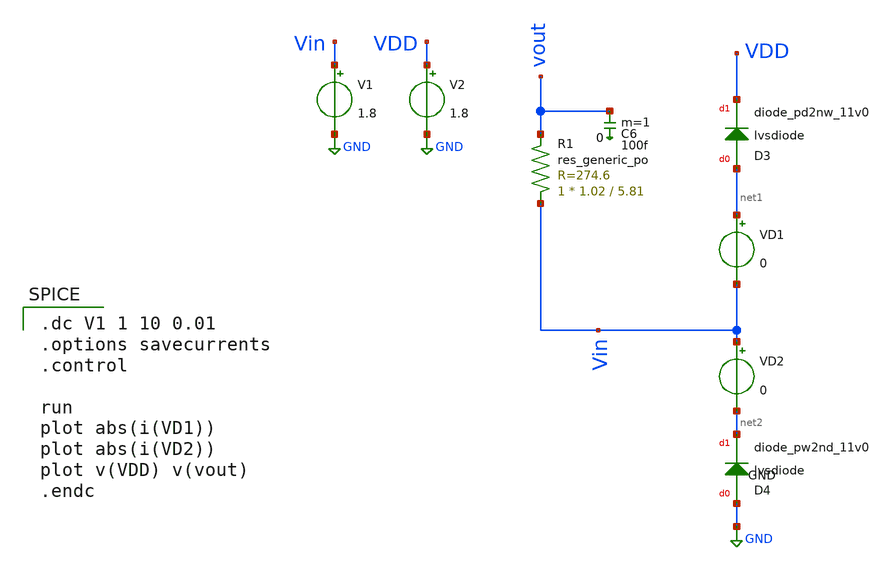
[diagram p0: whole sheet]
** sch_path: sky130_cells/ESD_Diode/TB_Flatten_Pins.sch
**.subckt TB_Flatten_Pins
VD1 net1 Vin 0
V1 Vin GND 1.8
V2 VDD GND 1.8
C6 vout 0 100f m=1
VD2 Vin net2 0
XR1 Vin vout sky130_fd_pr__res_generic_po W=1.02 L=5.81 m=1
D3 net1 VDD sky130_fd_pr__diode_pd2nw_11v0 area=4.40146e13
D4 GND net2 sky130_fd_pr__diode_pw2nd_11v0 area=2.59996e13
**** begin user architecture code
 .lib /usr/local/share/pdk/sky130A/libs.tech/ngspice/sky130.lib.spice tt

.dc V1 1 10 0.01
.options savecurrents
.control

run
plot abs(i(VD1))
plot abs(i(VD2))
plot v(VDD) v(vout)
.endc

**** end user architecture code
**.ends
.GLOBAL GND
.end
